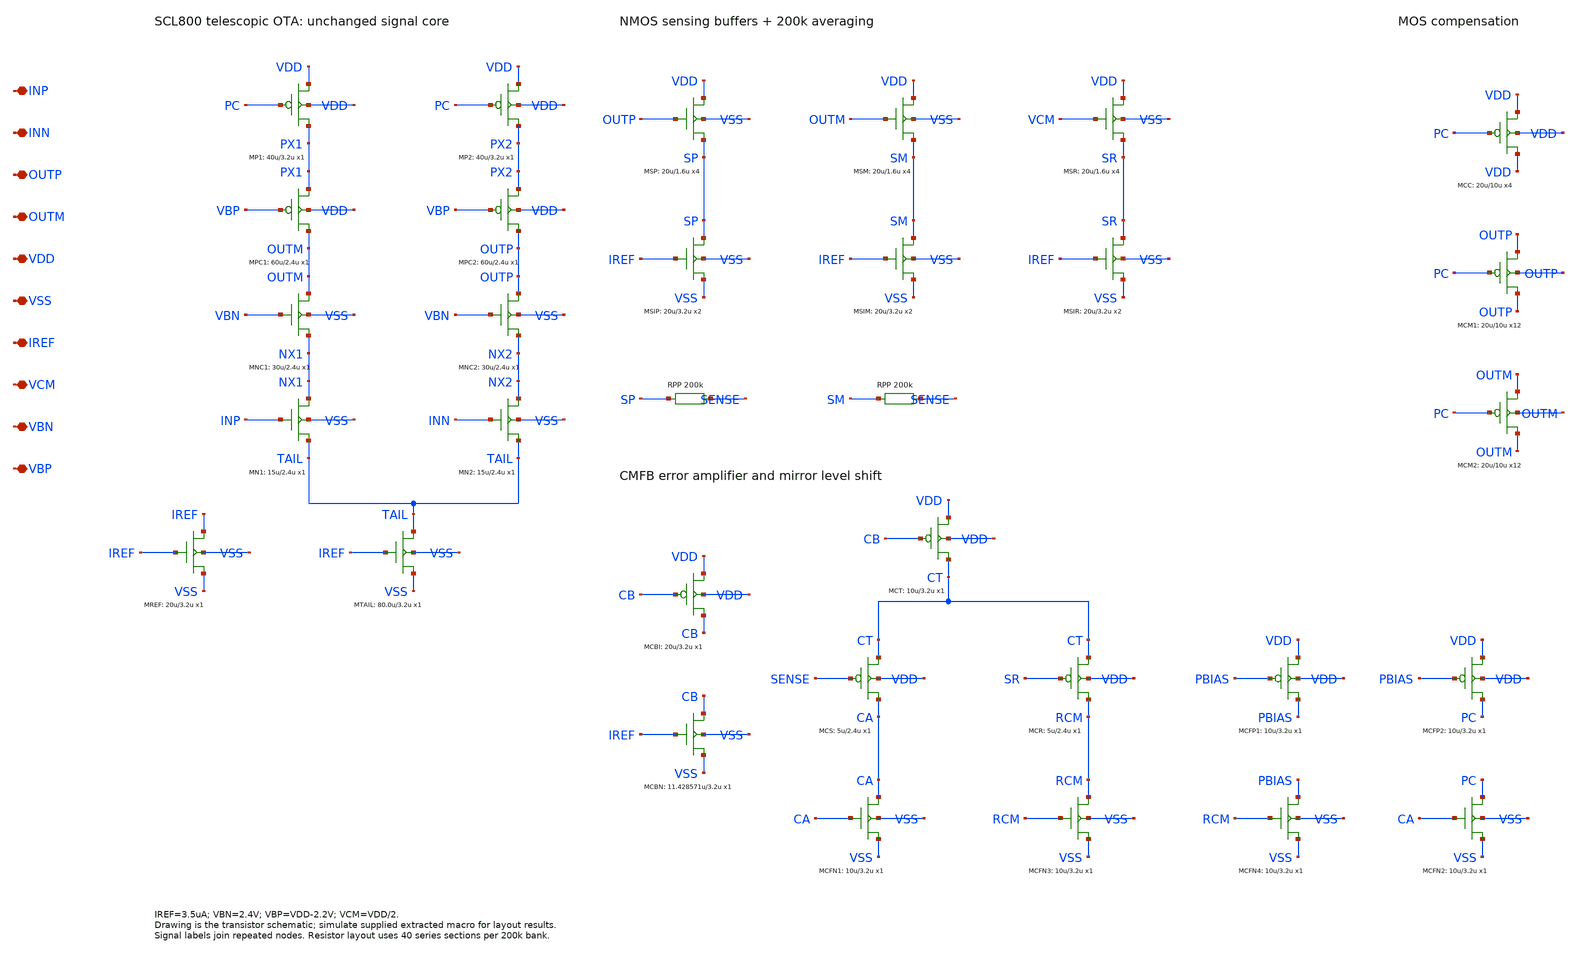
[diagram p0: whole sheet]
** sch_path: OTA/current_telescopic_cmfb_v2/designs/ota_telescopic_layout.sch
**.subckt ota_telescopic_layout INP INN OUTP OUTM VDD VSS IREF VCM VBN VBP
*.iopin INP
*.iopin INN
*.iopin OUTP
*.iopin OUTM
*.iopin VDD
*.iopin VSS
*.iopin IREF
*.iopin VCM
*.iopin VBN
*.iopin VBP
MSP VDD OUTP SP VSS N w=20u l=1.6u AD=90p AS=90p PD=49u PS=49u m=4
MSM VDD OUTM SM VSS N w=20u l=1.6u AD=90p AS=90p PD=49u PS=49u m=4
MSR VDD VCM SR VSS N w=20u l=1.6u AD=90p AS=90p PD=49u PS=49u m=4
MSIP SP IREF VSS VSS N w=20u l=3.2u AD=90p AS=90p PD=49u PS=49u m=2
MSIM SM IREF VSS VSS N w=20u l=3.2u AD=90p AS=90p PD=49u PS=49u m=2
MSIR SR IREF VSS VSS N w=20u l=3.2u AD=90p AS=90p PD=49u PS=49u m=2
MCBI CB CB VDD VDD P w=20u l=3.2u AD=90p AS=90p PD=49u PS=49u m=1
MCBN CB IREF VSS VSS N w=11.428571u l=3.2u AD=51.4286p AS=51.4286p PD=31.8571u PS=31.8571u m=1
MCC VDD PC VDD VDD P w=20u l=10u AD=90p AS=90p PD=49u PS=49u m=4
MCM1 OUTP PC OUTP OUTP P w=20u l=10u AD=90p AS=90p PD=49u PS=49u m=12
MCM2 OUTM PC OUTM OUTM P w=20u l=10u AD=90p AS=90p PD=49u PS=49u m=12
MTAIL TAIL IREF VSS VSS N w=80.0u l=3.2u AD=360p AS=360p PD=169u PS=169u m=1
MN1 NX1 INP TAIL VSS N w=15u l=2.4u AD=67.5p AS=67.5p PD=39u PS=39u m=1
MN2 NX2 INN TAIL VSS N w=15u l=2.4u AD=67.5p AS=67.5p PD=39u PS=39u m=1
MNC1 OUTM VBN NX1 VSS N w=30u l=2.4u AD=135p AS=135p PD=69u PS=69u m=1
MNC2 OUTP VBN NX2 VSS N w=30u l=2.4u AD=135p AS=135p PD=69u PS=69u m=1
MPC1 OUTM VBP PX1 VDD P w=60u l=2.4u AD=270p AS=270p PD=129u PS=129u m=1
MPC2 OUTP VBP PX2 VDD P w=60u l=2.4u AD=270p AS=270p PD=129u PS=129u m=1
MP1 PX1 PC VDD VDD P w=40u l=3.2u AD=180p AS=180p PD=89u PS=89u m=1
MP2 PX2 PC VDD VDD P w=40u l=3.2u AD=180p AS=180p PD=89u PS=89u m=1
MCS CA SENSE CT VDD P w=5u l=2.4u AD=22.5p AS=22.5p PD=19u PS=19u m=1
MCR RCM SR CT VDD P w=5u l=2.4u AD=22.5p AS=22.5p PD=19u PS=19u m=1
MCT CT CB VDD VDD P w=10u l=3.2u AD=45p AS=45p PD=29u PS=29u m=1
MCFN1 CA CA VSS VSS N w=10u l=3.2u AD=45p AS=45p PD=29u PS=29u m=1
MCFN2 PC CA VSS VSS N w=10u l=3.2u AD=45p AS=45p PD=29u PS=29u m=1
MCFN3 RCM RCM VSS VSS N w=10u l=3.2u AD=45p AS=45p PD=29u PS=29u m=1
MCFN4 PBIAS RCM VSS VSS N w=10u l=3.2u AD=45p AS=45p PD=29u PS=29u m=1
MCFP1 PBIAS PBIAS VDD VDD P w=10u l=3.2u AD=45p AS=45p PD=29u PS=29u m=1
MCFP2 PC PBIAS VDD VDD P w=10u l=3.2u AD=45p AS=45p PD=29u PS=29u m=1
MREF IREF IREF VSS VSS N w=20u l=3.2u AD=90p AS=90p PD=49u PS=49u m=1
XSP SP SENSE RPP W=2.4u L=17142.857143u
XSM SM SENSE RPP W=2.4u L=17142.857143u
**.ends
.end
